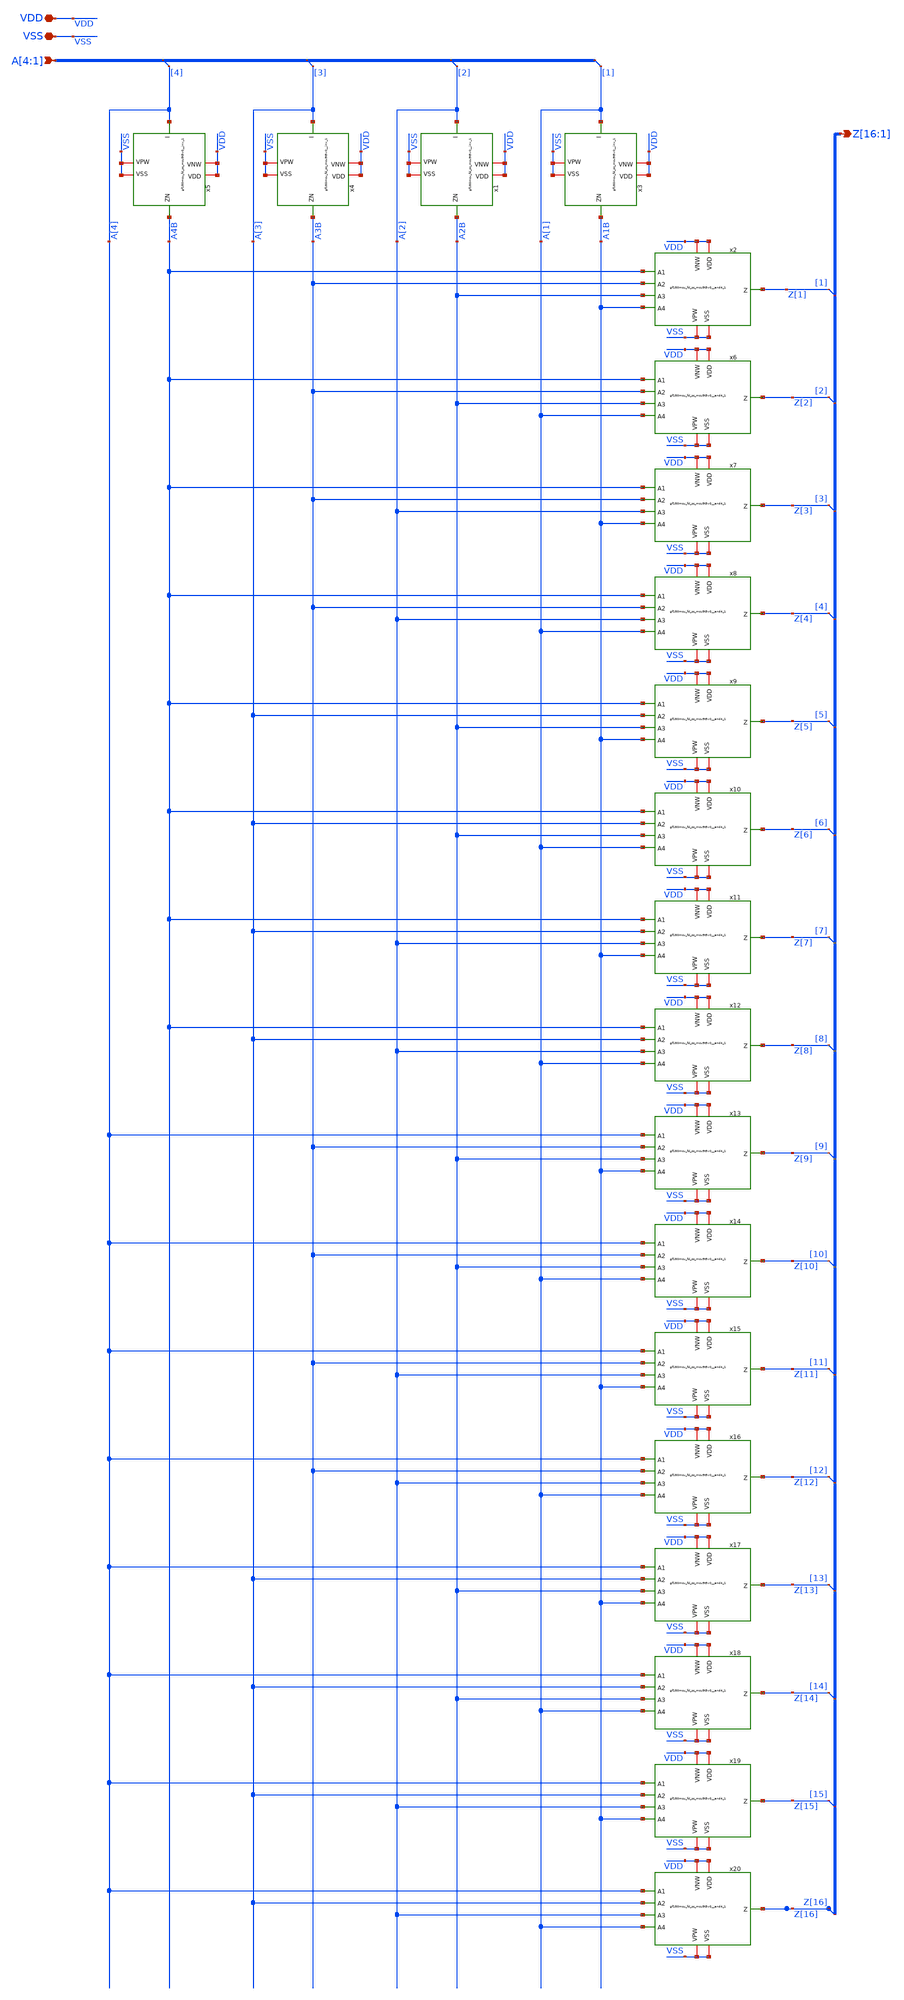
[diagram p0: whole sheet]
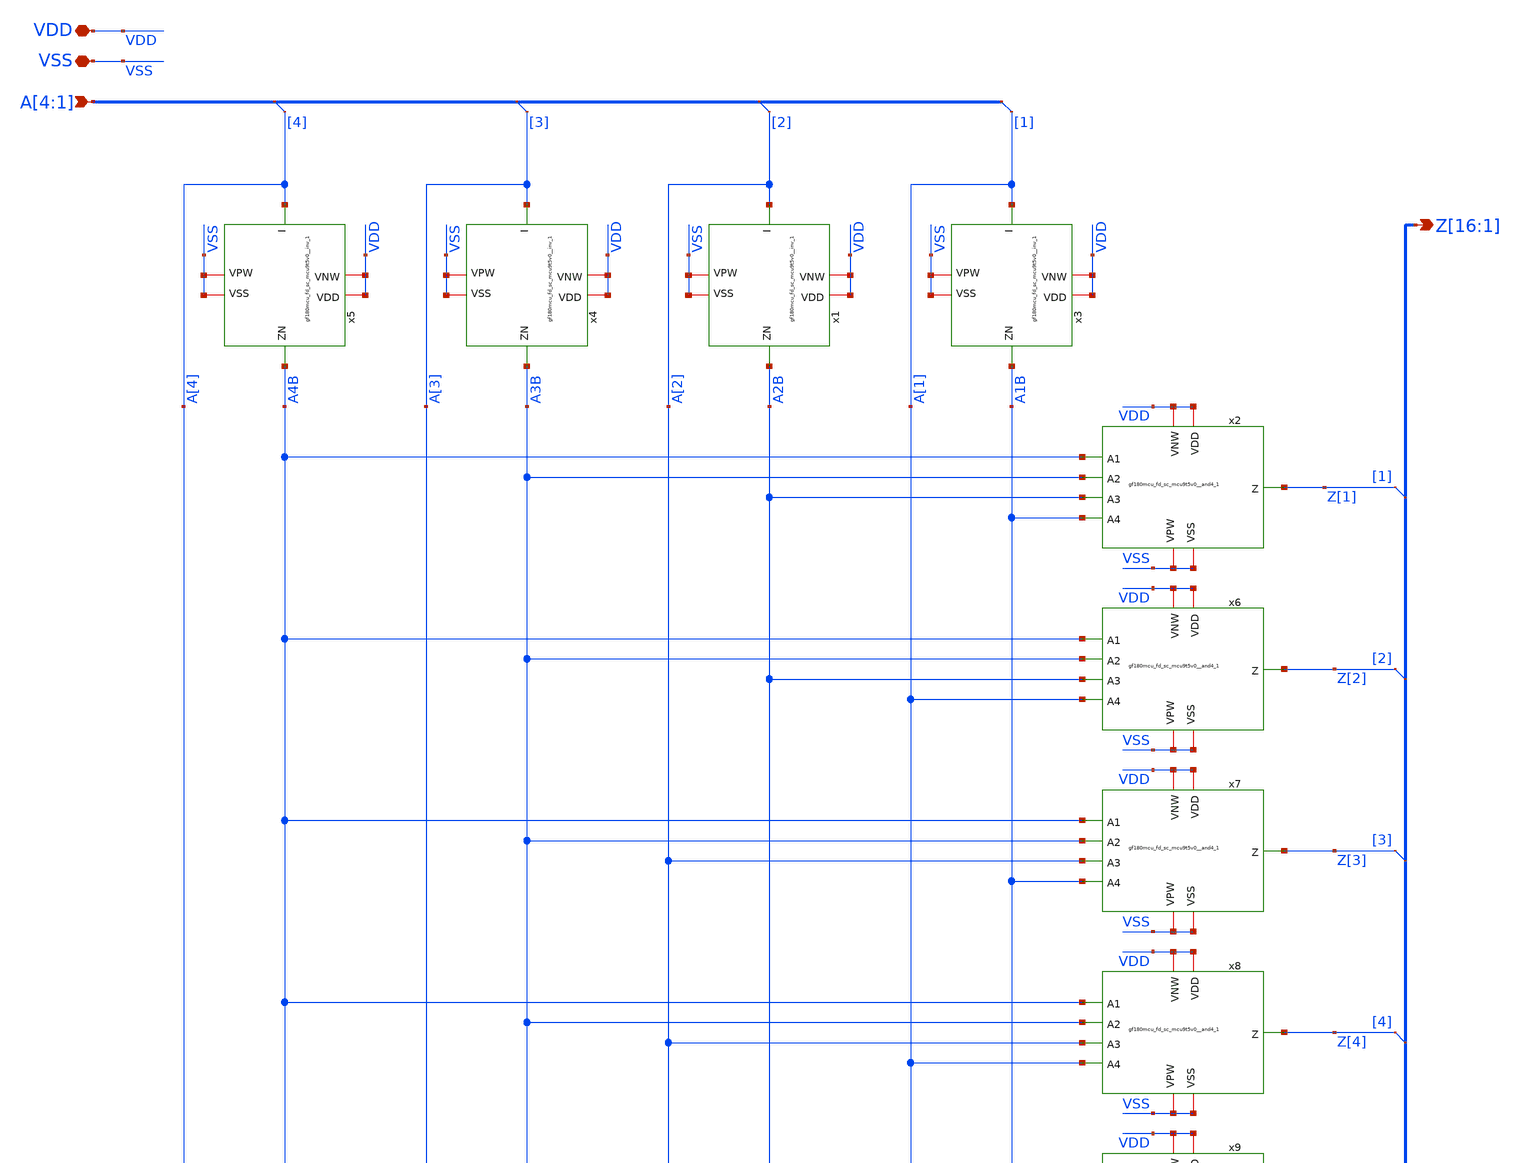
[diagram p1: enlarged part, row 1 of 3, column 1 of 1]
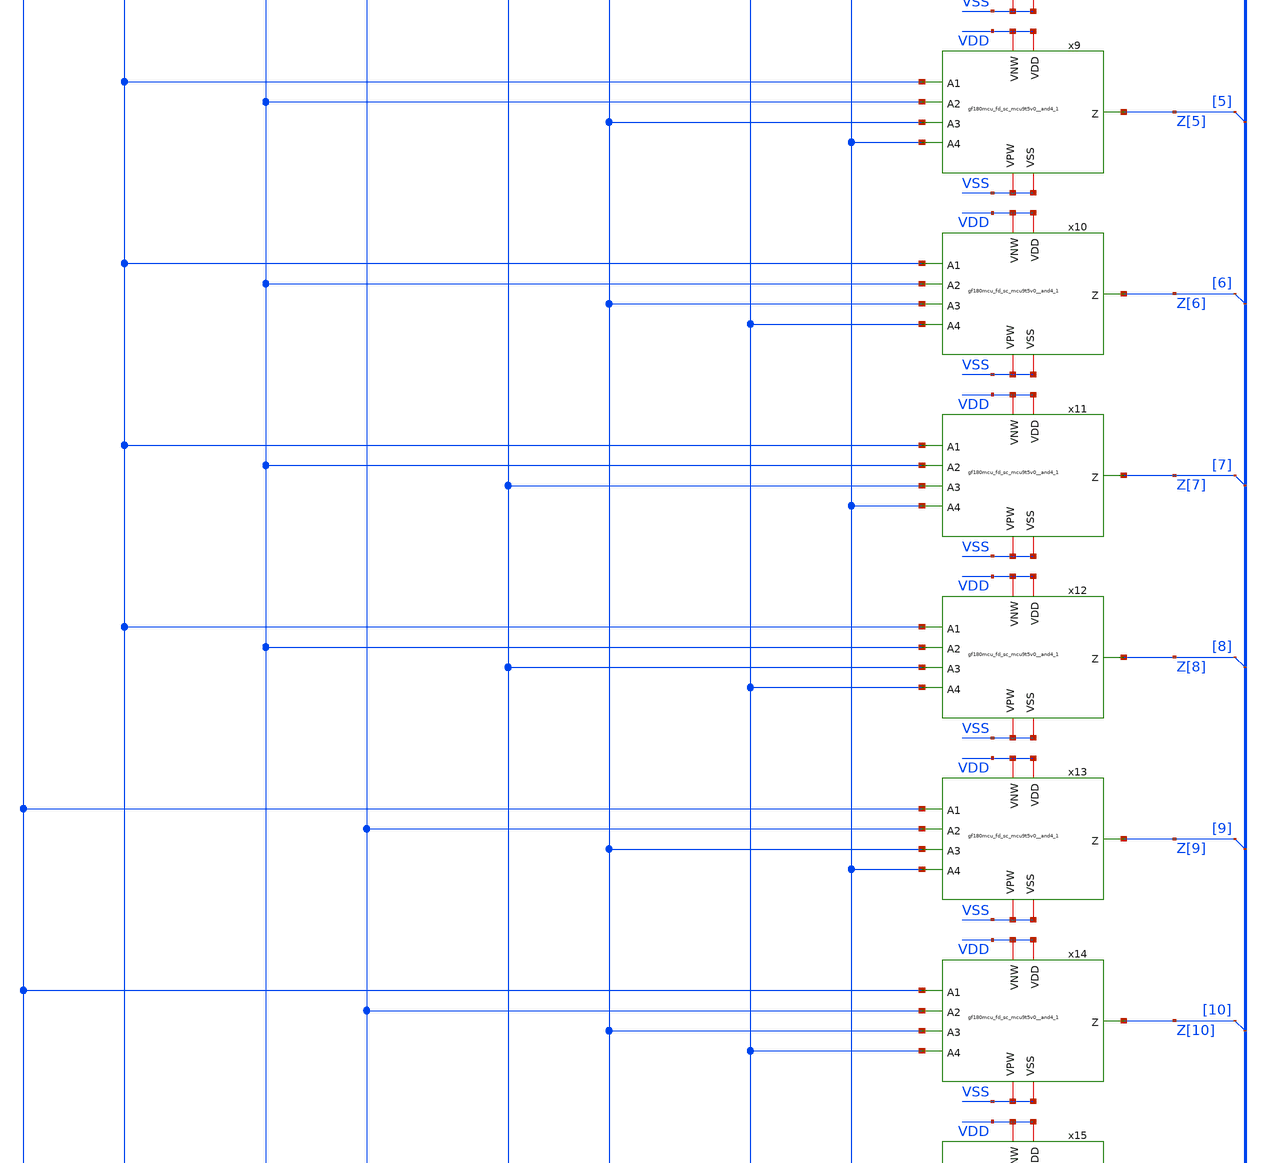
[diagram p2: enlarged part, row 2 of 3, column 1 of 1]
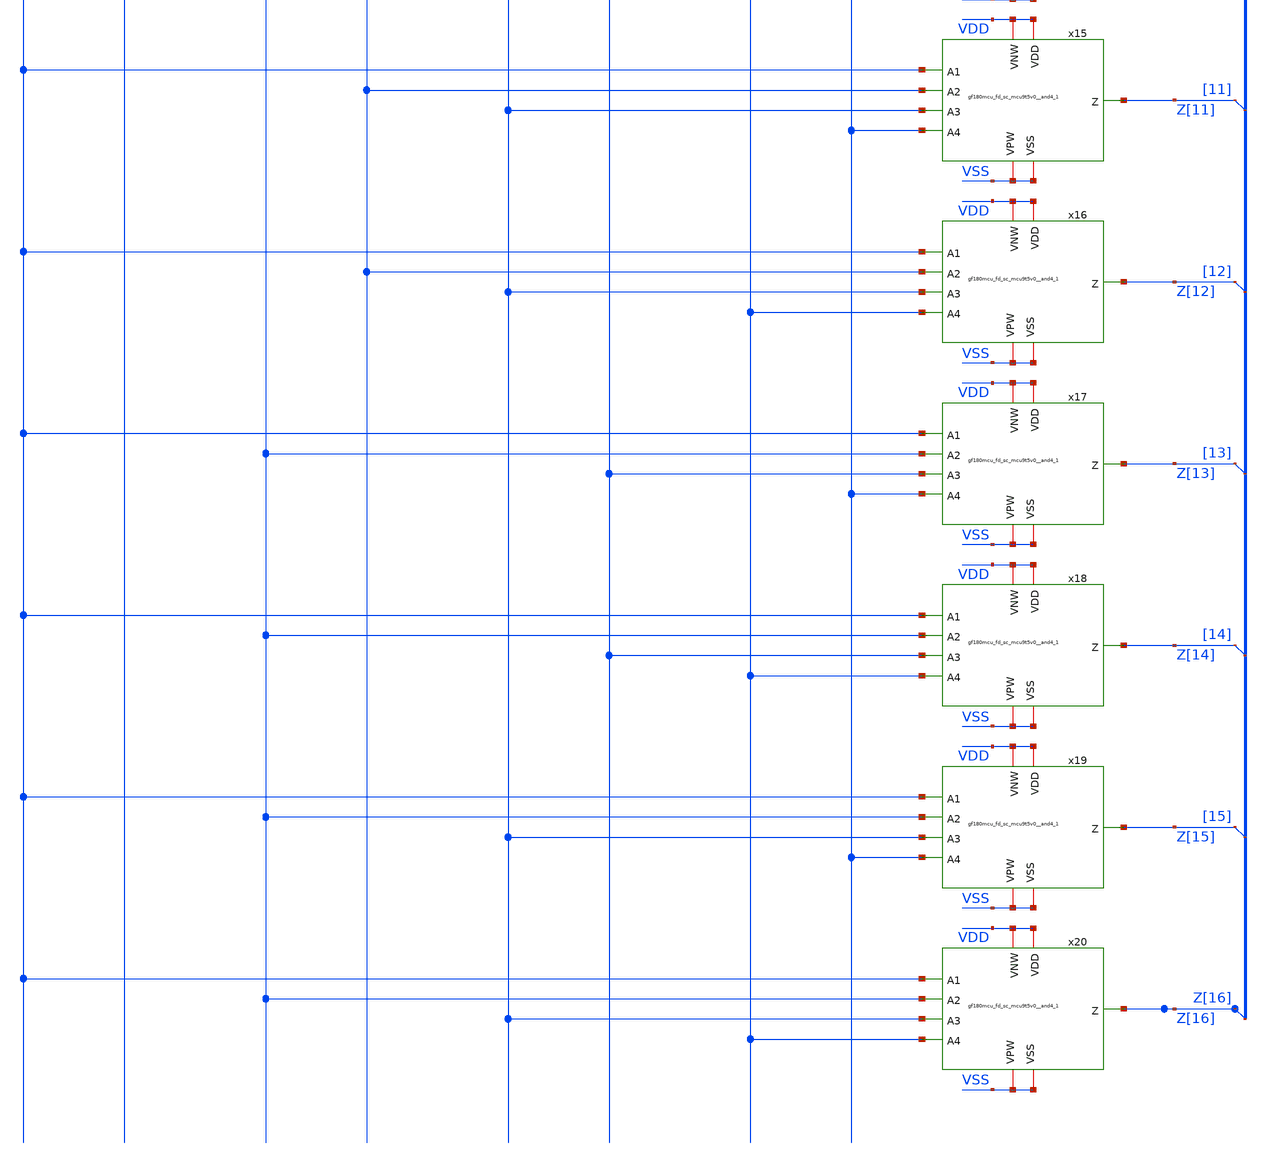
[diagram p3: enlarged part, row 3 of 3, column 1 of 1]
** sch_path: xschem/ip_line_mux.sch
**.subckt ip_line_mux A[4],A[3],A[2],A[1] VDD VSS
*+ Z[16],Z[15],Z[14],Z[13],Z[12],Z[11],Z[10],Z[9],Z[8],Z[7],Z[6],Z[5],Z[4],Z[3],Z[2],Z[1]
*.ipin A[4],A[3],A[2],A[1]
*.iopin VDD
*.iopin VSS
*.opin Z[16],Z[15],Z[14],Z[13],Z[12],Z[11],Z[10],Z[9],Z[8],Z[7],Z[6],Z[5],Z[4],Z[3],Z[2],Z[1]
x1 A[2] A2B VDD VDD VSS VSS gf180mcu_fd_sc_mcu9t5v0__inv_1
x2 A4B A3B A2B A1B Z[1] VDD VDD VSS VSS gf180mcu_fd_sc_mcu9t5v0__and4_1
x3 A[1] A1B VDD VDD VSS VSS gf180mcu_fd_sc_mcu9t5v0__inv_1
x4 A[3] A3B VDD VDD VSS VSS gf180mcu_fd_sc_mcu9t5v0__inv_1
x5 A[4] A4B VDD VDD VSS VSS gf180mcu_fd_sc_mcu9t5v0__inv_1
* tap: A[4:1] --> A[4]
* tap: A[4:1] --> A[3]
* tap: A[4:1] --> A[2]
* tap: A[4:1] --> A[1]
* tap: Z[16:1] --> Z[1]
* tap: Z[16:1] --> Z[2]
* tap: Z[16:1] --> Z[3]
* tap: Z[16:1] --> Z[4]
* tap: Z[16:1] --> Z[5]
* tap: Z[16:1] --> Z[6]
* tap: Z[16:1] --> Z[7]
* tap: Z[16:1] --> Z[8]
* tap: Z[16:1] --> Z[9]
* tap: Z[16:1] --> Z[10]
* tap: Z[16:1] --> Z[11]
* tap: Z[16:1] --> Z[12]
* tap: Z[16:1] --> Z[13]
* tap: Z[16:1] --> Z[14]
* tap: Z[16:1] --> Z[15]
* tap: Z[16:1] --> Z[16]
x6 A4B A3B A2B A[1] Z[2] VDD VDD VSS VSS gf180mcu_fd_sc_mcu9t5v0__and4_1
x7 A4B A3B A[2] A1B Z[3] VDD VDD VSS VSS gf180mcu_fd_sc_mcu9t5v0__and4_1
x8 A4B A3B A[2] A[1] Z[4] VDD VDD VSS VSS gf180mcu_fd_sc_mcu9t5v0__and4_1
x9 A4B A[3] A2B A1B Z[5] VDD VDD VSS VSS gf180mcu_fd_sc_mcu9t5v0__and4_1
x10 A4B A[3] A2B A[1] Z[6] VDD VDD VSS VSS gf180mcu_fd_sc_mcu9t5v0__and4_1
x11 A4B A[3] A[2] A1B Z[7] VDD VDD VSS VSS gf180mcu_fd_sc_mcu9t5v0__and4_1
x12 A4B A[3] A[2] A[1] Z[8] VDD VDD VSS VSS gf180mcu_fd_sc_mcu9t5v0__and4_1
x13 A[4] A3B A2B A1B Z[9] VDD VDD VSS VSS gf180mcu_fd_sc_mcu9t5v0__and4_1
x14 A[4] A3B A2B A[1] Z[10] VDD VDD VSS VSS gf180mcu_fd_sc_mcu9t5v0__and4_1
x15 A[4] A3B A[2] A1B Z[11] VDD VDD VSS VSS gf180mcu_fd_sc_mcu9t5v0__and4_1
x16 A[4] A3B A[2] A[1] Z[12] VDD VDD VSS VSS gf180mcu_fd_sc_mcu9t5v0__and4_1
x17 A[4] A[3] A2B A1B Z[13] VDD VDD VSS VSS gf180mcu_fd_sc_mcu9t5v0__and4_1
x18 A[4] A[3] A2B A[1] Z[14] VDD VDD VSS VSS gf180mcu_fd_sc_mcu9t5v0__and4_1
x19 A[4] A[3] A[2] A1B Z[15] VDD VDD VSS VSS gf180mcu_fd_sc_mcu9t5v0__and4_1
x20 A[4] A[3] A[2] A[1] Z[16] VDD VDD VSS VSS gf180mcu_fd_sc_mcu9t5v0__and4_1
**.ends
.end
